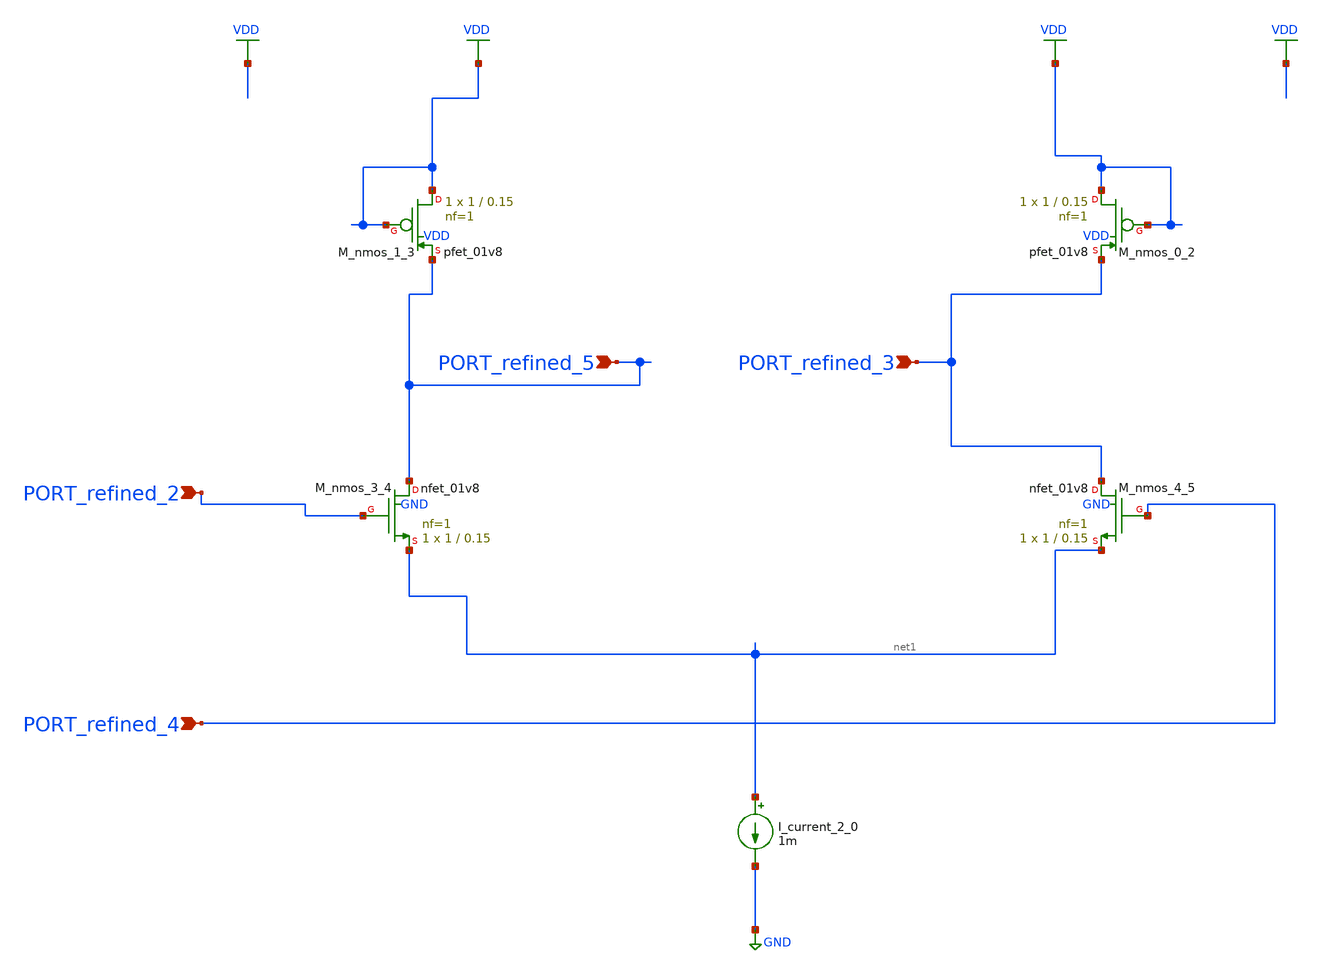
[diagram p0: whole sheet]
** sch_path: schematics/AMSNet/808.sch
**.subckt 808 PORT_refined_2 PORT_refined_5 PORT_refined_3 PORT_refined_4
*.ipin PORT_refined_2
*.ipin PORT_refined_5
*.ipin PORT_refined_3
*.ipin PORT_refined_4
I_current_2_0 net1 GND 1m
XM_nmos_0_2 VDD VDD PORT_refined_3 VDD sky130_fd_pr__pfet_01v8 L=0.15 W=1 nf=1 ad='int((1 + 1)/2) * 1 / 1 * 0.29'
+ as='int((1 + 2)/2) * 1 / 1 * 0.29' pd='2*int((1 + 1)/2) * (1 / 1 + 0.29)' ps='2*int((1 + 2)/2) * (1 / 1 + 0.29)'
+ nrd='0.29 / 1 ' nrs='0.29 / 1 ' sa=0 sb=0 sd=0 mult=1 m=1
XM_nmos_1_3 VDD VDD PORT_refined_5 VDD sky130_fd_pr__pfet_01v8 L=0.15 W=1 nf=1 ad='int((1 + 1)/2) * 1 / 1 * 0.29'
+ as='int((1 + 2)/2) * 1 / 1 * 0.29' pd='2*int((1 + 1)/2) * (1 / 1 + 0.29)' ps='2*int((1 + 2)/2) * (1 / 1 + 0.29)'
+ nrd='0.29 / 1 ' nrs='0.29 / 1 ' sa=0 sb=0 sd=0 mult=1 m=1
XM_nmos_3_4 PORT_refined_5 PORT_refined_2 net1 GND sky130_fd_pr__nfet_01v8 L=0.15 W=1 nf=1 ad='int((1 + 1)/2) * 1 / 1 * 0.29'
+ as='int((1 + 2)/2) * 1 / 1 * 0.29' pd='2*int((1 + 1)/2) * (1 / 1 + 0.29)' ps='2*int((1 + 2)/2) * (1 / 1 + 0.29)'
+ nrd='0.29 / 1 ' nrs='0.29 / 1 ' sa=0 sb=0 sd=0 mult=1 m=1
XM_nmos_4_5 PORT_refined_3 PORT_refined_4 net1 GND sky130_fd_pr__nfet_01v8 L=0.15 W=1 nf=1 ad='int((1 + 1)/2) * 1 / 1 * 0.29'
+ as='int((1 + 2)/2) * 1 / 1 * 0.29' pd='2*int((1 + 1)/2) * (1 / 1 + 0.29)' ps='2*int((1 + 2)/2) * (1 / 1 + 0.29)'
+ nrd='0.29 / 1 ' nrs='0.29 / 1 ' sa=0 sb=0 sd=0 mult=1 m=1
**.ends
.GLOBAL GND
.GLOBAL VDD
.end
